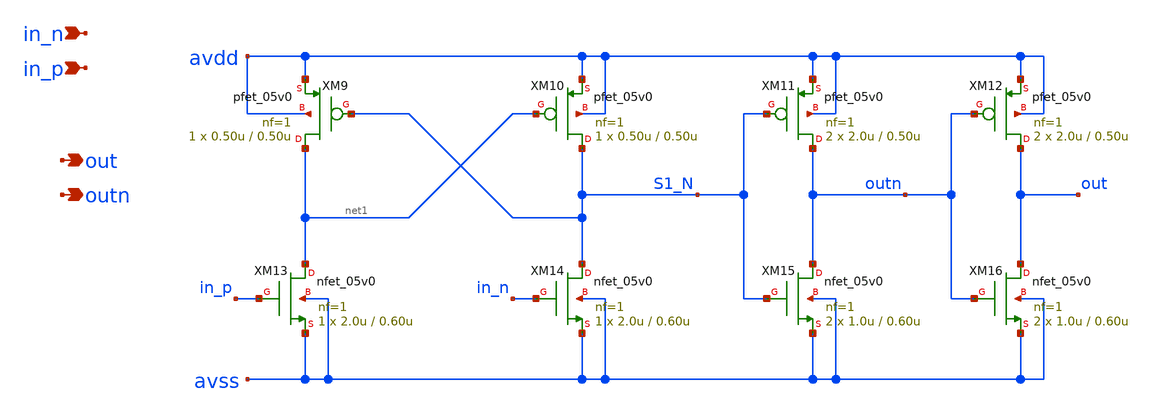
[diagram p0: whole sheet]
** sch_path: xschem/sw_lvl_shift.sch
**.subckt sw_lvl_shift in_n in_p out outn
*.ipin in_n
*.ipin in_p
*.opin out
*.opin outn
XM9 net1 S1_N avdd avdd pfet_05v0 L=0.50u W=0.50u nf=1 ad='int((nf+1)/2) * W/nf * 0.18u' as='int((nf+2)/2) * W/nf * 0.18u'
+ pd='2*int((nf+1)/2) * (W/nf + 0.18u)' ps='2*int((nf+2)/2) * (W/nf + 0.18u)' nrd='0.18u / W' nrs='0.18u / W'
+ sa=0 sb=0 sd=0 m=1 par=1
XM10 S1_N net1 avdd avdd pfet_05v0 L=0.50u W=0.50u nf=1 ad='int((nf+1)/2) * W/nf * 0.18u' as='int((nf+2)/2) * W/nf * 0.18u'
+ pd='2*int((nf+1)/2) * (W/nf + 0.18u)' ps='2*int((nf+2)/2) * (W/nf + 0.18u)' nrd='0.18u / W' nrs='0.18u / W'
+ sa=0 sb=0 sd=0 m=1 par=1
XM11 outn S1_N avdd avdd pfet_05v0 L=0.50u W=2.0u nf=1 ad='int((nf+1)/2) * W/nf * 0.18u' as='int((nf+2)/2) * W/nf * 0.18u'
+ pd='2*int((nf+1)/2) * (W/nf + 0.18u)' ps='2*int((nf+2)/2) * (W/nf + 0.18u)' nrd='0.18u / W' nrs='0.18u / W'
+ sa=0 sb=0 sd=0 m=2 par=2
XM12 out outn avdd avdd pfet_05v0 L=0.50u W=2.0u nf=1 ad='int((nf+1)/2) * W/nf * 0.18u' as='int((nf+2)/2) * W/nf * 0.18u'
+ pd='2*int((nf+1)/2) * (W/nf + 0.18u)' ps='2*int((nf+2)/2) * (W/nf + 0.18u)' nrd='0.18u / W' nrs='0.18u / W'
+ sa=0 sb=0 sd=0 m=2 par=2
XM13 net1 in_p avss avss nfet_05v0 L=0.60u W=2.0u nf=1 ad='int((nf+1)/2) * W/nf * 0.18u' as='int((nf+2)/2) * W/nf * 0.18u'
+ pd='2*int((nf+1)/2) * (W/nf + 0.18u)' ps='2*int((nf+2)/2) * (W/nf + 0.18u)' nrd='0.18u / W' nrs='0.18u / W'
+ sa=0 sb=0 sd=0 m=1
XM14 S1_N in_n avss avss nfet_05v0 L=0.60u W=2.0u nf=1 ad='int((nf+1)/2) * W/nf * 0.18u' as='int((nf+2)/2) * W/nf * 0.18u'
+ pd='2*int((nf+1)/2) * (W/nf + 0.18u)' ps='2*int((nf+2)/2) * (W/nf + 0.18u)' nrd='0.18u / W' nrs='0.18u / W'
+ sa=0 sb=0 sd=0 m=1
XM15 outn S1_N avss avss nfet_05v0 L=0.60u W=1.0u nf=1 ad='int((nf+1)/2) * W/nf * 0.18u' as='int((nf+2)/2) * W/nf * 0.18u'
+ pd='2*int((nf+1)/2) * (W/nf + 0.18u)' ps='2*int((nf+2)/2) * (W/nf + 0.18u)' nrd='0.18u / W' nrs='0.18u / W'
+ sa=0 sb=0 sd=0 m=2
XM16 out outn avss avss nfet_05v0 L=0.60u W=1.0u nf=1 ad='int((nf+1)/2) * W/nf * 0.18u' as='int((nf+2)/2) * W/nf * 0.18u'
+ pd='2*int((nf+1)/2) * (W/nf + 0.18u)' ps='2*int((nf+2)/2) * (W/nf + 0.18u)' nrd='0.18u / W' nrs='0.18u / W'
+ sa=0 sb=0 sd=0 m=2
**.ends
.end
